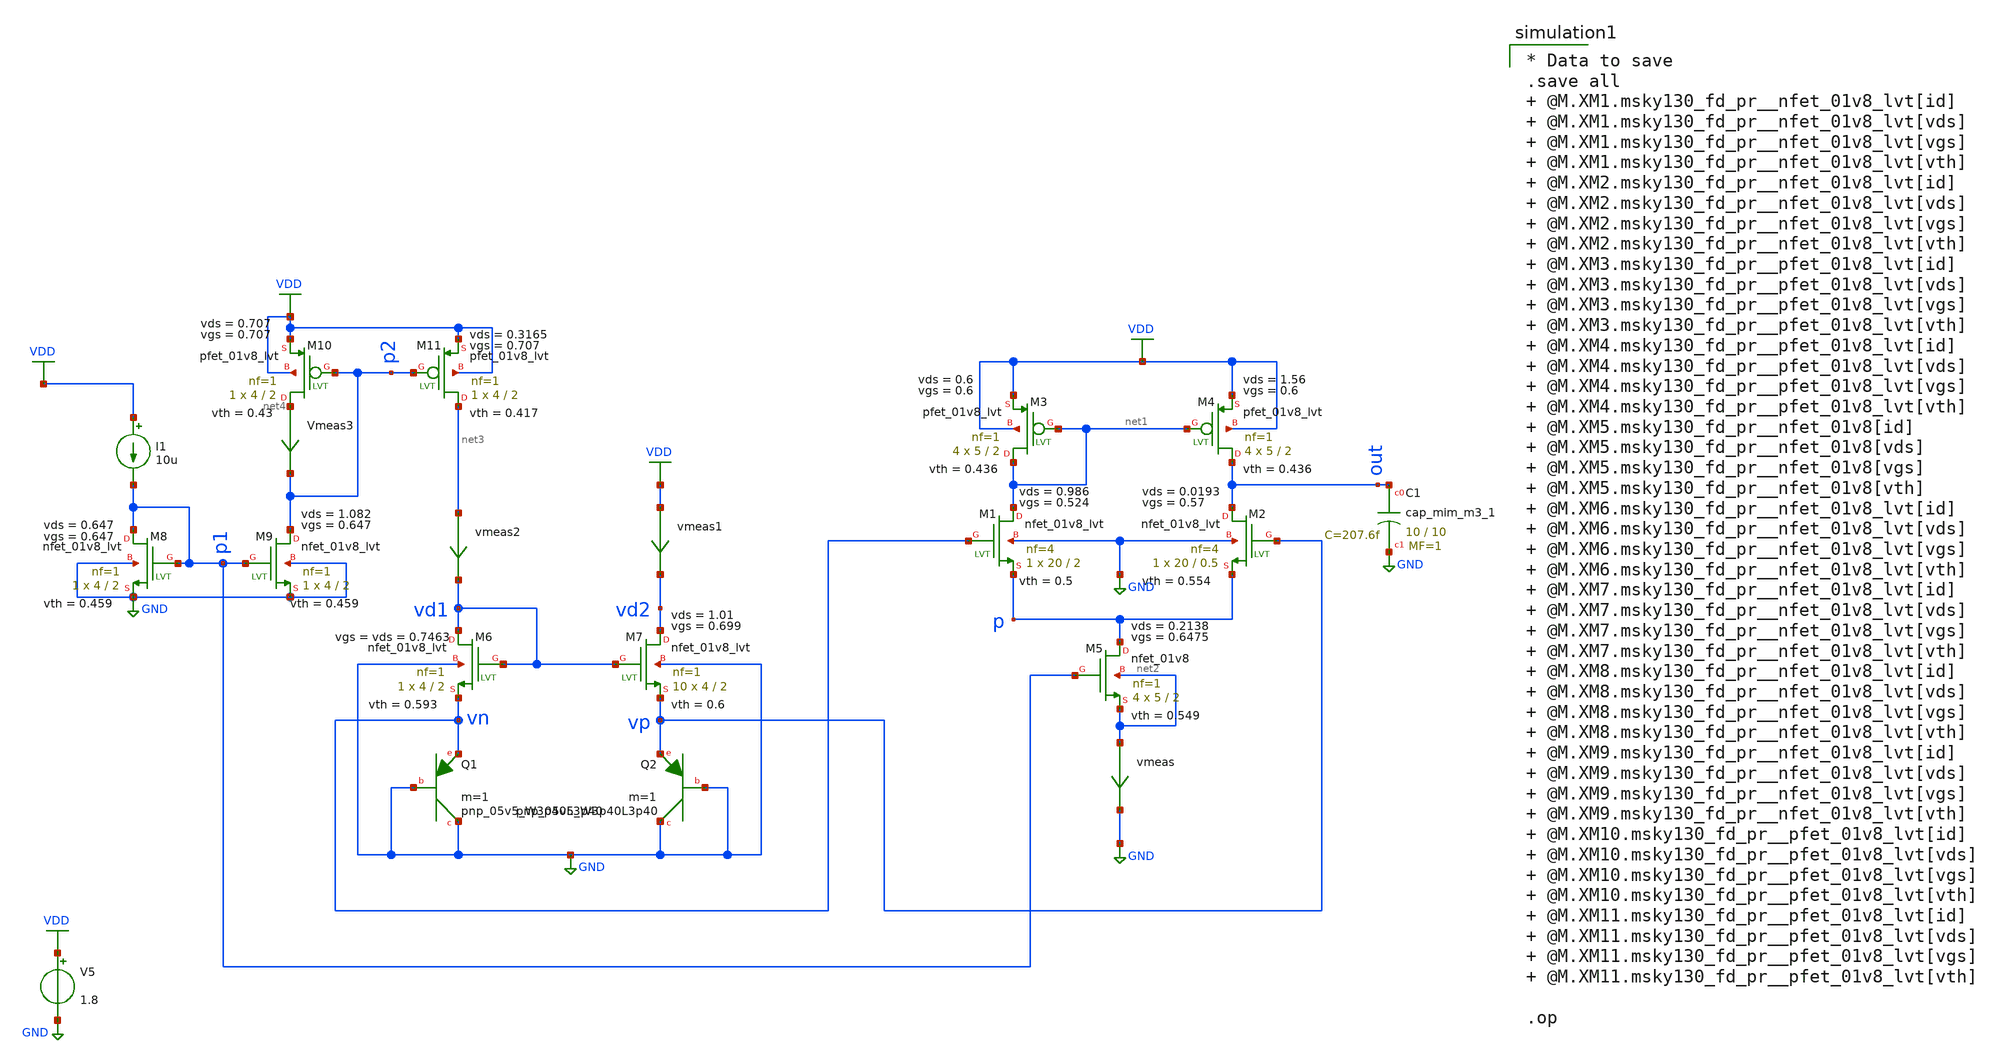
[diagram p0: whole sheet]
** sch_path: ANOTHER_SOLUTIONS_CONSIDERED/ANOTHER_BIAS_FOR_TEMPERATURE_SENSOR/TEMPERATURE_SENSOR/XSCHEM/Temp_Sensor_unbalanced_tb_op.sch
**.subckt Temp_Sensor_unbalanced_tb_op
XM1 net1 vn p GND sky130_fd_pr__nfet_01v8_lvt L=2 W=20 nf=4 ad='int((nf+1)/2) * W/nf * 0.29' as='int((nf+2)/2) * W/nf * 0.29'
+ pd='2*int((nf+1)/2) * (W/nf + 0.29)' ps='2*int((nf+2)/2) * (W/nf + 0.29)' nrd='0.29 / W' nrs='0.29 / W'
+ sa=0 sb=0 sd=0 mult=1 m=1
XM2 out vp p GND sky130_fd_pr__nfet_01v8_lvt L=0.5 W=20 nf=4 ad='int((nf+1)/2) * W/nf * 0.29' as='int((nf+2)/2) * W/nf * 0.29'
+ pd='2*int((nf+1)/2) * (W/nf + 0.29)' ps='2*int((nf+2)/2) * (W/nf + 0.29)' nrd='0.29 / W' nrs='0.29 / W'
+ sa=0 sb=0 sd=0 mult=1 m=1
vmeas net2 GND 0
.save i(vmeas)
XM5 p p1 net2 net2 sky130_fd_pr__nfet_01v8 L=2 W=5 nf=1 ad='int((nf+1)/2) * W/nf * 0.29' as='int((nf+2)/2) * W/nf * 0.29'
+ pd='2*int((nf+1)/2) * (W/nf + 0.29)' ps='2*int((nf+2)/2) * (W/nf + 0.29)' nrd='0.29 / W' nrs='0.29 / W'
+ sa=0 sb=0 sd=0 mult=4 m=4
XM3 net1 net1 VDD VDD sky130_fd_pr__pfet_01v8_lvt L=2 W=5 nf=1 ad='int((nf+1)/2) * W/nf * 0.29' as='int((nf+2)/2) * W/nf * 0.29'
+ pd='2*int((nf+1)/2) * (W/nf + 0.29)' ps='2*int((nf+2)/2) * (W/nf + 0.29)' nrd='0.29 / W' nrs='0.29 / W'
+ sa=0 sb=0 sd=0 mult=4 m=4
XM4 out net1 VDD VDD sky130_fd_pr__pfet_01v8_lvt L=2 W=5 nf=1 ad='int((nf+1)/2) * W/nf * 0.29' as='int((nf+2)/2) * W/nf * 0.29'
+ pd='2*int((nf+1)/2) * (W/nf + 0.29)' ps='2*int((nf+2)/2) * (W/nf + 0.29)' nrd='0.29 / W' nrs='0.29 / W'
+ sa=0 sb=0 sd=0 mult=4 m=4
XC1 out GND sky130_fd_pr__cap_mim_m3_1 W=10 L=10 MF=1 m=1
XM6 vd1 vd1 vn GND sky130_fd_pr__nfet_01v8_lvt L=2 W=4 nf=1 ad='int((nf+1)/2) * W/nf * 0.29' as='int((nf+2)/2) * W/nf * 0.29'
+ pd='2*int((nf+1)/2) * (W/nf + 0.29)' ps='2*int((nf+2)/2) * (W/nf + 0.29)' nrd='0.29 / W' nrs='0.29 / W'
+ sa=0 sb=0 sd=0 mult=1 m=1
XQ1 GND GND vn sky130_fd_pr__pnp_05v5_W3p40L3p40 m=1
XM7 vd2 vd1 vp GND sky130_fd_pr__nfet_01v8_lvt L=2 W=4 nf=1 ad='int((nf+1)/2) * W/nf * 0.29' as='int((nf+2)/2) * W/nf * 0.29'
+ pd='2*int((nf+1)/2) * (W/nf + 0.29)' ps='2*int((nf+2)/2) * (W/nf + 0.29)' nrd='0.29 / W' nrs='0.29 / W'
+ sa=0 sb=0 sd=0 mult=10 m=10
XQ2 GND GND vp sky130_fd_pr__pnp_05v5_W3p40L3p40 m=1
V5 VDD GND 1.8
vmeas1 VDD vd2 0
.save i(vmeas1)
vmeas2 net3 vd1 0
.save i(vmeas2)
I1 VDD p1 10u
XM8 p1 p1 GND GND sky130_fd_pr__nfet_01v8_lvt L=2 W=4 nf=1 ad='int((nf+1)/2) * W/nf * 0.29' as='int((nf+2)/2) * W/nf * 0.29'
+ pd='2*int((nf+1)/2) * (W/nf + 0.29)' ps='2*int((nf+2)/2) * (W/nf + 0.29)' nrd='0.29 / W' nrs='0.29 / W'
+ sa=0 sb=0 sd=0 mult=1 m=1
XM9 p2 p1 GND GND sky130_fd_pr__nfet_01v8_lvt L=2 W=4 nf=1 ad='int((nf+1)/2) * W/nf * 0.29' as='int((nf+2)/2) * W/nf * 0.29'
+ pd='2*int((nf+1)/2) * (W/nf + 0.29)' ps='2*int((nf+2)/2) * (W/nf + 0.29)' nrd='0.29 / W' nrs='0.29 / W'
+ sa=0 sb=0 sd=0 mult=1 m=1
XM10 net4 p2 VDD VDD sky130_fd_pr__pfet_01v8_lvt L=2 W=4 nf=1 ad='int((nf+1)/2) * W/nf * 0.29' as='int((nf+2)/2) * W/nf * 0.29'
+ pd='2*int((nf+1)/2) * (W/nf + 0.29)' ps='2*int((nf+2)/2) * (W/nf + 0.29)' nrd='0.29 / W' nrs='0.29 / W'
+ sa=0 sb=0 sd=0 mult=1 m=1
XM11 net3 p2 VDD VDD sky130_fd_pr__pfet_01v8_lvt L=2 W=4 nf=1 ad='int((nf+1)/2) * W/nf * 0.29' as='int((nf+2)/2) * W/nf * 0.29'
+ pd='2*int((nf+1)/2) * (W/nf + 0.29)' ps='2*int((nf+2)/2) * (W/nf + 0.29)' nrd='0.29 / W' nrs='0.29 / W'
+ sa=0 sb=0 sd=0 mult=1 m=1
Vmeas3 net4 p2 0
.save i(vmeas3)
**** begin user architecture code

* Data to save
.save all  @M.XM1.msky130_fd_pr__nfet_01v8_lvt[id]  @M.XM1.msky130_fd_pr__nfet_01v8_lvt[vds]  @M.XM1.msky130_fd_pr__nfet_01v8_lvt[vgs]  @M.XM1.msky130_fd_pr__nfet_01v8_lvt[vth]  @M.XM2.msky130_fd_pr__nfet_01v8_lvt[id]  @M.XM2.msky130_fd_pr__nfet_01v8_lvt[vds]  @M.XM2.msky130_fd_pr__nfet_01v8_lvt[vgs]  @M.XM2.msky130_fd_pr__nfet_01v8_lvt[vth]  @M.XM3.msky130_fd_pr__pfet_01v8_lvt[id]  @M.XM3.msky130_fd_pr__pfet_01v8_lvt[vds]  @M.XM3.msky130_fd_pr__pfet_01v8_lvt[vgs]  @M.XM3.msky130_fd_pr__pfet_01v8_lvt[vth]  @M.XM4.msky130_fd_pr__pfet_01v8_lvt[id]  @M.XM4.msky130_fd_pr__pfet_01v8_lvt[vds]  @M.XM4.msky130_fd_pr__pfet_01v8_lvt[vgs]  @M.XM4.msky130_fd_pr__pfet_01v8_lvt[vth]  @M.XM5.msky130_fd_pr__nfet_01v8[id]  @M.XM5.msky130_fd_pr__nfet_01v8[vds]  @M.XM5.msky130_fd_pr__nfet_01v8[vgs]  @M.XM5.msky130_fd_pr__nfet_01v8[vth]  @M.XM6.msky130_fd_pr__nfet_01v8_lvt[id]  @M.XM6.msky130_fd_pr__nfet_01v8_lvt[vds]  @M.XM6.msky130_fd_pr__nfet_01v8_lvt[vgs]  @M.XM6.msky130_fd_pr__nfet_01v8_lvt[vth]  @M.XM7.msky130_fd_pr__nfet_01v8_lvt[id]  @M.XM7.msky130_fd_pr__nfet_01v8_lvt[vds]  @M.XM7.msky130_fd_pr__nfet_01v8_lvt[vgs]  @M.XM7.msky130_fd_pr__nfet_01v8_lvt[vth]  @M.XM8.msky130_fd_pr__nfet_01v8_lvt[id]  @M.XM8.msky130_fd_pr__nfet_01v8_lvt[vds]  @M.XM8.msky130_fd_pr__nfet_01v8_lvt[vgs]  @M.XM8.msky130_fd_pr__nfet_01v8_lvt[vth]  @M.XM9.msky130_fd_pr__nfet_01v8_lvt[id]  @M.XM9.msky130_fd_pr__nfet_01v8_lvt[vds]  @M.XM9.msky130_fd_pr__nfet_01v8_lvt[vgs]  @M.XM9.msky130_fd_pr__nfet_01v8_lvt[vth]  @M.XM10.msky130_fd_pr__pfet_01v8_lvt[id]  @M.XM10.msky130_fd_pr__pfet_01v8_lvt[vds]  @M.XM10.msky130_fd_pr__pfet_01v8_lvt[vgs]  @M.XM10.msky130_fd_pr__pfet_01v8_lvt[vth]  @M.XM11.msky130_fd_pr__pfet_01v8_lvt[id]  @M.XM11.msky130_fd_pr__pfet_01v8_lvt[vds]  @M.XM11.msky130_fd_pr__pfet_01v8_lvt[vgs]  @M.XM11.msky130_fd_pr__pfet_01v8_lvt[vth]

.op



** opencircuitdesign pdks install
.lib $::SKYWATER_MODELS/sky130.lib.spice tt


**** end user architecture code
**.ends
.GLOBAL VDD
.GLOBAL GND
.end
